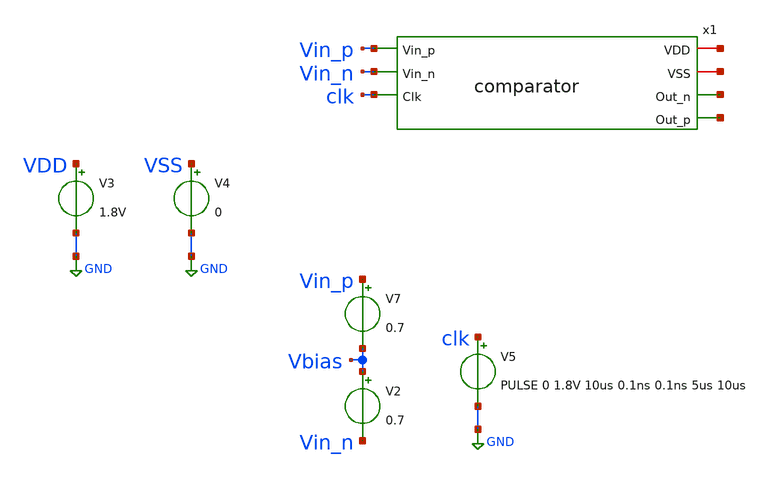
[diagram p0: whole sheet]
** sch_path: xschem/tests/dummy_tests/stepping_tran_test.sch
**.subckt stepping_tran_test
V3 VDD GND 1.8V
V4 VSS GND 0
x1 net1 net2 Vin_p net3 Vin_n net4 clk comparator
V2 Vbias Vin_n 0.7
V5 clk GND PULSE 0 1.8V 10us 0.1ns 0.1ns 5us 10us
V7 Vin_p Vbias 0.7
**** begin user architecture code
 .lib $::SKYWATER_MODELS/sky130.lib.spice tt
.include $::SKYWATER_STDCELLS/sky130_fd_sc_hd.spice


.options acct list
.temp 25
*vvcc VDD 0 dc 1.8
*vvss VSS 0 0
.control
tran 0.1u 400u
*plot RST_PLS clk+2 Pulse+4
write pulse_generator_test.raw
.endc


**** end user architecture code
**.ends

* expanding   symbol:  src/comparator/comparator.sym # of pins=7
** sym_path: xschem/src/comparator/comparator.sym
** sch_path: xschem/src/comparator/comparator.sch
.subckt comparator VDD VSS Vin_p Out_n Vin_n Out_p Clk
*.iopin VDD
*.iopin VSS
*.ipin Vin_p
*.opin Out_n
*.ipin Vin_n
*.opin Out_p
*.ipin Clk
XM1 Pre_Amp_n Clk VDD VSS sky130_fd_pr__pfet_01v8 L=0.15 W=1 nf=1 ad='int((nf+1)/2) * W/nf * 0.29' as='int((nf+2)/2) * W/nf * 0.29'
+ pd='2*int((nf+1)/2) * (W/nf + 0.29)' ps='2*int((nf+2)/2) * (W/nf + 0.29)' nrd='0.29 / W' nrs='0.29 / W'
+ sa=0 sb=0 sd=0 mult=1 m=1
XM2 Pre_Amp_p Clk VDD VSS sky130_fd_pr__pfet_01v8 L=0.15 W=1 nf=1 ad='int((nf+1)/2) * W/nf * 0.29' as='int((nf+2)/2) * W/nf * 0.29'
+ pd='2*int((nf+1)/2) * (W/nf + 0.29)' ps='2*int((nf+2)/2) * (W/nf + 0.29)' nrd='0.29 / W' nrs='0.29 / W'
+ sa=0 sb=0 sd=0 mult=1 m=1
XM3 Pre_Amp_p Vin_p net1 VSS sky130_fd_pr__nfet_01v8 L=0.15 W=1 nf=1 ad='int((nf+1)/2) * W/nf * 0.29'
+ as='int((nf+2)/2) * W/nf * 0.29' pd='2*int((nf+1)/2) * (W/nf + 0.29)' ps='2*int((nf+2)/2) * (W/nf + 0.29)'
+ nrd='0.29 / W' nrs='0.29 / W' sa=0 sb=0 sd=0 mult=1 m=1
XM4 Pre_Amp_n Vin_n net1 VSS sky130_fd_pr__nfet_01v8 L=0.15 W=1 nf=1 ad='int((nf+1)/2) * W/nf * 0.29'
+ as='int((nf+2)/2) * W/nf * 0.29' pd='2*int((nf+1)/2) * (W/nf + 0.29)' ps='2*int((nf+2)/2) * (W/nf + 0.29)'
+ nrd='0.29 / W' nrs='0.29 / W' sa=0 sb=0 sd=0 mult=1 m=1
XM5 net3 Out_p VDD VSS sky130_fd_pr__pfet_01v8 L=0.15 W=1 nf=1 ad='int((nf+1)/2) * W/nf * 0.29' as='int((nf+2)/2) * W/nf * 0.29'
+ pd='2*int((nf+1)/2) * (W/nf + 0.29)' ps='2*int((nf+2)/2) * (W/nf + 0.29)' nrd='0.29 / W' nrs='0.29 / W'
+ sa=0 sb=0 sd=0 mult=1 m=1
XM6 net2 Out_n VDD VSS sky130_fd_pr__pfet_01v8 L=0.15 W=1 nf=1 ad='int((nf+1)/2) * W/nf * 0.29' as='int((nf+2)/2) * W/nf * 0.29'
+ pd='2*int((nf+1)/2) * (W/nf + 0.29)' ps='2*int((nf+2)/2) * (W/nf + 0.29)' nrd='0.29 / W' nrs='0.29 / W'
+ sa=0 sb=0 sd=0 mult=1 m=1
XM7 net2 Pre_Amp_p Out_p VSS sky130_fd_pr__nfet_01v8 L=0.15 W=1 nf=1 ad='int((nf+1)/2) * W/nf * 0.29'
+ as='int((nf+2)/2) * W/nf * 0.29' pd='2*int((nf+1)/2) * (W/nf + 0.29)' ps='2*int((nf+2)/2) * (W/nf + 0.29)'
+ nrd='0.29 / W' nrs='0.29 / W' sa=0 sb=0 sd=0 mult=1 m=1
XM8 net3 Pre_Amp_n Out_n VSS sky130_fd_pr__nfet_01v8 L=0.15 W=1 nf=1 ad='int((nf+1)/2) * W/nf * 0.29'
+ as='int((nf+2)/2) * W/nf * 0.29' pd='2*int((nf+1)/2) * (W/nf + 0.29)' ps='2*int((nf+2)/2) * (W/nf + 0.29)'
+ nrd='0.29 / W' nrs='0.29 / W' sa=0 sb=0 sd=0 mult=1 m=1
XM9 net1 Clk VSS VSS sky130_fd_pr__nfet_01v8 L=0.15 W=1 nf=1 ad='int((nf+1)/2) * W/nf * 0.29' as='int((nf+2)/2) * W/nf * 0.29'
+ pd='2*int((nf+1)/2) * (W/nf + 0.29)' ps='2*int((nf+2)/2) * (W/nf + 0.29)' nrd='0.29 / W' nrs='0.29 / W'
+ sa=0 sb=0 sd=0 mult=1 m=1
XM10 Pre_Amp_n Vin_n net1 VSS sky130_fd_pr__nfet_01v8 L=0.15 W=1 nf=1 ad='int((nf+1)/2) * W/nf * 0.29'
+ as='int((nf+2)/2) * W/nf * 0.29' pd='2*int((nf+1)/2) * (W/nf + 0.29)' ps='2*int((nf+2)/2) * (W/nf + 0.29)'
+ nrd='0.29 / W' nrs='0.29 / W' sa=0 sb=0 sd=0 mult=1 m=1
XM11 Out_n Clk_n VSS VSS sky130_fd_pr__nfet_01v8 L=0.15 W=1 nf=1 ad='int((nf+1)/2) * W/nf * 0.29' as='int((nf+2)/2) * W/nf * 0.29'
+ pd='2*int((nf+1)/2) * (W/nf + 0.29)' ps='2*int((nf+2)/2) * (W/nf + 0.29)' nrd='0.29 / W' nrs='0.29 / W'
+ sa=0 sb=0 sd=0 mult=1 m=1
XM12 Out_n Out_p VSS VSS sky130_fd_pr__nfet_01v8 L=0.15 W=1 nf=1 ad='int((nf+1)/2) * W/nf * 0.29' as='int((nf+2)/2) * W/nf * 0.29'
+ pd='2*int((nf+1)/2) * (W/nf + 0.29)' ps='2*int((nf+2)/2) * (W/nf + 0.29)' nrd='0.29 / W' nrs='0.29 / W'
+ sa=0 sb=0 sd=0 mult=1 m=1
XM13 Out_p Out_n VSS VSS sky130_fd_pr__nfet_01v8 L=0.15 W=1 nf=1 ad='int((nf+1)/2) * W/nf * 0.29' as='int((nf+2)/2) * W/nf * 0.29'
+ pd='2*int((nf+1)/2) * (W/nf + 0.29)' ps='2*int((nf+2)/2) * (W/nf + 0.29)' nrd='0.29 / W' nrs='0.29 / W'
+ sa=0 sb=0 sd=0 mult=1 m=1
XM14 Out_p Clk_n VSS VSS sky130_fd_pr__nfet_01v8 L=0.15 W=1 nf=1 ad='int((nf+1)/2) * W/nf * 0.29' as='int((nf+2)/2) * W/nf * 0.29'
+ pd='2*int((nf+1)/2) * (W/nf + 0.29)' ps='2*int((nf+2)/2) * (W/nf + 0.29)' nrd='0.29 / W' nrs='0.29 / W'
+ sa=0 sb=0 sd=0 mult=1 m=1
XM15 Clk_n Clk VDD VSS sky130_fd_pr__pfet_01v8 L=0.15 W=1 nf=1 ad='int((nf+1)/2) * W/nf * 0.29' as='int((nf+2)/2) * W/nf * 0.29'
+ pd='2*int((nf+1)/2) * (W/nf + 0.29)' ps='2*int((nf+2)/2) * (W/nf + 0.29)' nrd='0.29 / W' nrs='0.29 / W'
+ sa=0 sb=0 sd=0 mult=1 m=1
XM16 Clk_n Clk VSS VSS sky130_fd_pr__nfet_01v8 L=0.15 W=1 nf=1 ad='int((nf+1)/2) * W/nf * 0.29' as='int((nf+2)/2) * W/nf * 0.29'
+ pd='2*int((nf+1)/2) * (W/nf + 0.29)' ps='2*int((nf+2)/2) * (W/nf + 0.29)' nrd='0.29 / W' nrs='0.29 / W'
+ sa=0 sb=0 sd=0 mult=1 m=1
.ends

.GLOBAL GND
.end
